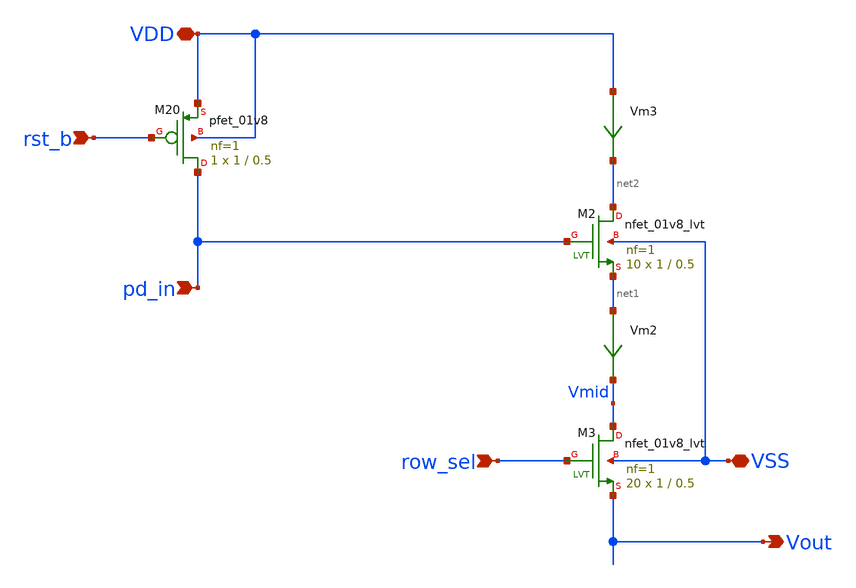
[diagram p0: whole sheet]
** sch_path: xschem/cmos_imager/3T.sch
**.subckt 3T Vout rst_b pd_in VDD row_sel VSS
*.opin Vout
*.ipin rst_b
*.ipin pd_in
*.iopin VDD
*.ipin row_sel
*.iopin VSS
XM2 net2 pd_in net1 VSS sky130_fd_pr__nfet_01v8_lvt L=0.5 W=1 nf=1 ad='int((nf+1)/2) * W/nf * 0.29' as='int((nf+2)/2) * W/nf * 0.29'
+ pd='2*int((nf+1)/2) * (W/nf + 0.29)' ps='2*int((nf+2)/2) * (W/nf + 0.29)' nrd='0.29 / W' nrs='0.29 / W'
+ sa=0 sb=0 sd=0 mult=10 m=10
Vm2 net1 Vmid 0
.save i(vm2)
Vm3 VDD net2 0
.save i(vm3)
XM3 Vmid row_sel Vout VSS sky130_fd_pr__nfet_01v8_lvt L=0.5 W=1 nf=1 ad='int((nf+1)/2) * W/nf * 0.29'
+ as='int((nf+2)/2) * W/nf * 0.29' pd='2*int((nf+1)/2) * (W/nf + 0.29)' ps='2*int((nf+2)/2) * (W/nf + 0.29)'
+ nrd='0.29 / W' nrs='0.29 / W' sa=0 sb=0 sd=0 mult=20 m=20
XM20 pd_in rst_b VDD VDD sky130_fd_pr__pfet_01v8 L=0.5 W=1 nf=1 ad='int((nf+1)/2) * W/nf * 0.29' as='int((nf+2)/2) * W/nf * 0.29'
+ pd='2*int((nf+1)/2) * (W/nf + 0.29)' ps='2*int((nf+2)/2) * (W/nf + 0.29)' nrd='0.29 / W' nrs='0.29 / W'
+ sa=0 sb=0 sd=0 mult=1 m=1
**.ends
.end
